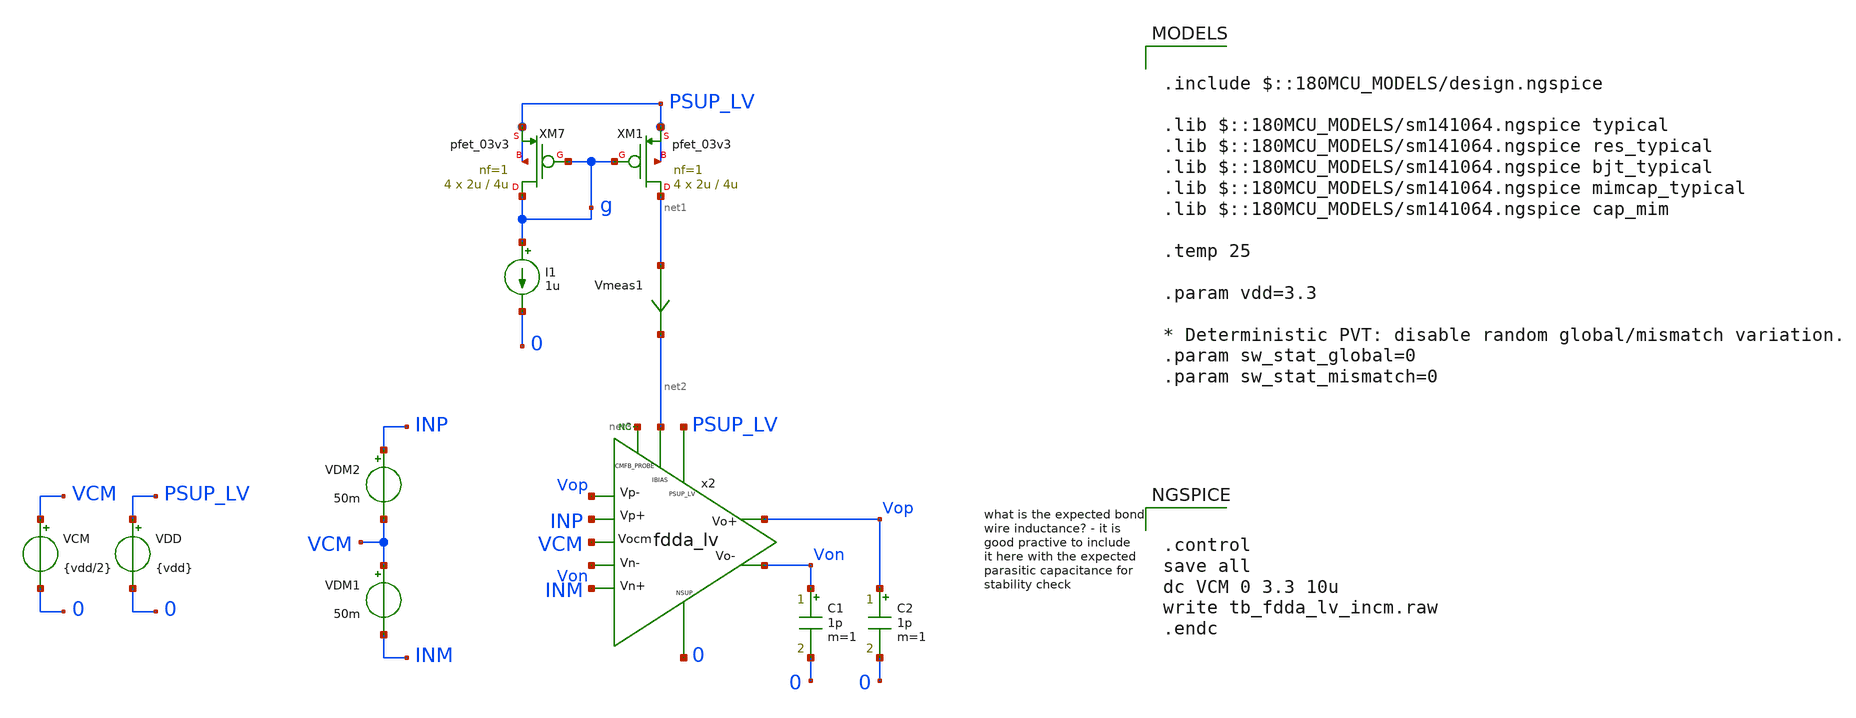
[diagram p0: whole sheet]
** sch_path: xschem/blocks/fdda_lv/tb_fdda_lv_incm.sch
**.subckt tb_fdda_lv_incm
C1 Von 0 1p m=1
x2 PSUP_LV Vop Von INM INP Vop Von net2 0 net3 VCM fdda_lv
VDD PSUP_LV 0 {vdd}
C2 Vop 0 1p m=1
VCM VCM 0 {vdd/2}
VDM2 INP VCM 50m
VDM1 VCM INM 50m
* noconn #net3
XM7 g g PSUP_LV PSUP_LV pfet_03v3 L=4u W=2u nf=1 ad='int((nf+1)/2) * W/nf * 0.18u' as='int((nf+2)/2) * W/nf * 0.18u'
+ pd='2*int((nf+1)/2) * (W/nf + 0.18u)' ps='2*int((nf+2)/2) * (W/nf + 0.18u)' nrd='0.18u / W' nrs='0.18u / W'
+ sa=0 sb=0 sd=0 m=4
XM1 net1 g PSUP_LV PSUP_LV pfet_03v3 L=4u W=2u nf=1 ad='int((nf+1)/2) * W/nf * 0.18u' as='int((nf+2)/2) * W/nf * 0.18u'
+ pd='2*int((nf+1)/2) * (W/nf + 0.18u)' ps='2*int((nf+2)/2) * (W/nf + 0.18u)' nrd='0.18u / W' nrs='0.18u / W'
+ sa=0 sb=0 sd=0 m=4
I1 g 0 1u
Vmeas1 net1 net2 0
.save i(vmeas1)
**** begin user architecture code

.include $::180MCU_MODELS/design.ngspice

.lib $::180MCU_MODELS/sm141064.ngspice typical
.lib $::180MCU_MODELS/sm141064.ngspice res_typical
.lib $::180MCU_MODELS/sm141064.ngspice bjt_typical
.lib $::180MCU_MODELS/sm141064.ngspice mimcap_typical
.lib $::180MCU_MODELS/sm141064.ngspice cap_mim

.temp 25

.param vdd=3.3

* Deterministic PVT: disable random global/mismatch variation.
.param sw_stat_global=0
.param sw_stat_mismatch=0



.control
save all
dc VCM 0 3.3 10u
write tb_fdda_lv_incm.raw
.endc


**** end user architecture code
**.ends
.end
